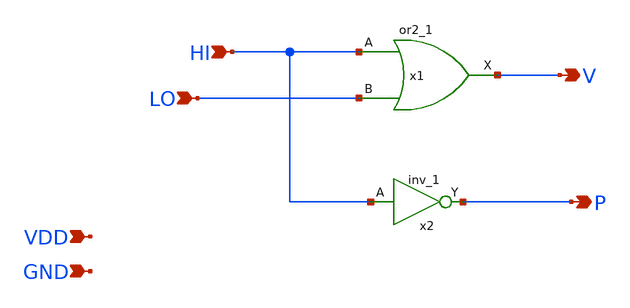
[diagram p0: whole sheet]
** sch_path: xschem/zlc2.sch
**.subckt zlc2 HI LO V P VDD GND
*.ipin HI
*.ipin LO
*.opin V
*.opin P
*.ipin VDD
*.ipin GND
x1 HI LO GND GND VDD VDD V sky130_fd_sc_hd__or2_1
x2 HI GND GND VDD VDD P sky130_fd_sc_hd__inv_1
**.ends
.end
